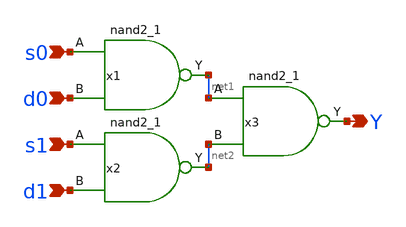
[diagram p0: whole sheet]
** sch_path: elements/logic/mux2.sch
**.subckt mux2 s0 d0 s1 d1 Y
*.ipin s0
*.ipin d0
*.ipin s1
*.ipin d1
*.opin Y
x1 s0 d0 VSS VSS VCC VCC net1 sky130_fd_sc_hd__nand2_1
x2 s1 d1 VSS VSS VCC VCC net2 sky130_fd_sc_hd__nand2_1
x3 net1 net2 VSS VSS VCC VCC Y sky130_fd_sc_hd__nand2_1
**.ends
.end
